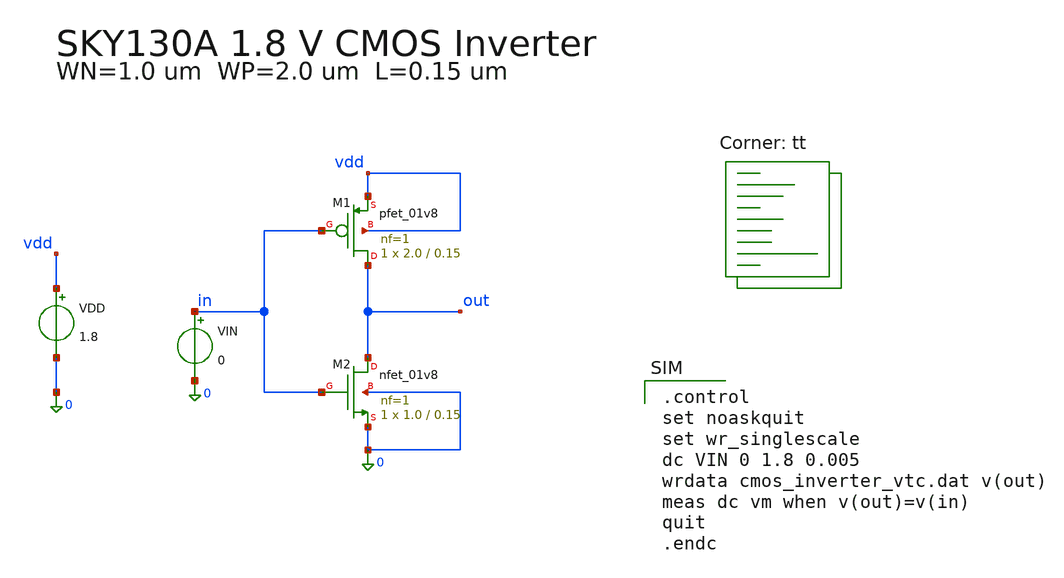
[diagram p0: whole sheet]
** sch_path: design/xschem/cmos_inverter.sch
**.subckt cmos_inverter
XM1 out in vdd vdd sky130_fd_pr__pfet_01v8 L=0.15 W=2.0 nf=1 ad='int((nf+1)/2) * W/nf * 0.29' as='int((nf+2)/2) * W/nf * 0.29'
+ pd='2*int((nf+1)/2) * (W/nf + 0.29)' ps='2*int((nf+2)/2) * (W/nf + 0.29)' nrd='0.29 / W' nrs='0.29 / W'
+ sa=0 sb=0 sd=0 mult=1 m=1
XM2 out in 0 0 sky130_fd_pr__nfet_01v8 L=0.15 W=1.0 nf=1 ad='int((1 + 1)/2) * 1.0 / 1 * 0.29' as='int((1 + 2)/2) * 1.0 / 1 * 0.29'
+ pd='2*int((1 + 1)/2) * (1.0 / 1 + 0.29)' ps='2*int((1 + 2)/2) * (1.0 / 1 + 0.29)' nrd='0.29 / 1.0 ' nrs='0.29 / 1.0 '
+ sa=0 sb=0 sd=0 mult=1 m=1
VDD vdd 0 1.8
.save i(vdd)
VIN in 0 0
**** begin user architecture code
.lib $::SKYWATER_MODELS/sky130.lib.spice tt

.control
set noaskquit
set wr_singlescale
dc VIN 0 1.8 0.005
wrdata cmos_inverter_vtc.dat v(out)
meas dc vm when v(out)=v(in)
quit
.endc

**** end user architecture code
**.ends
.end
